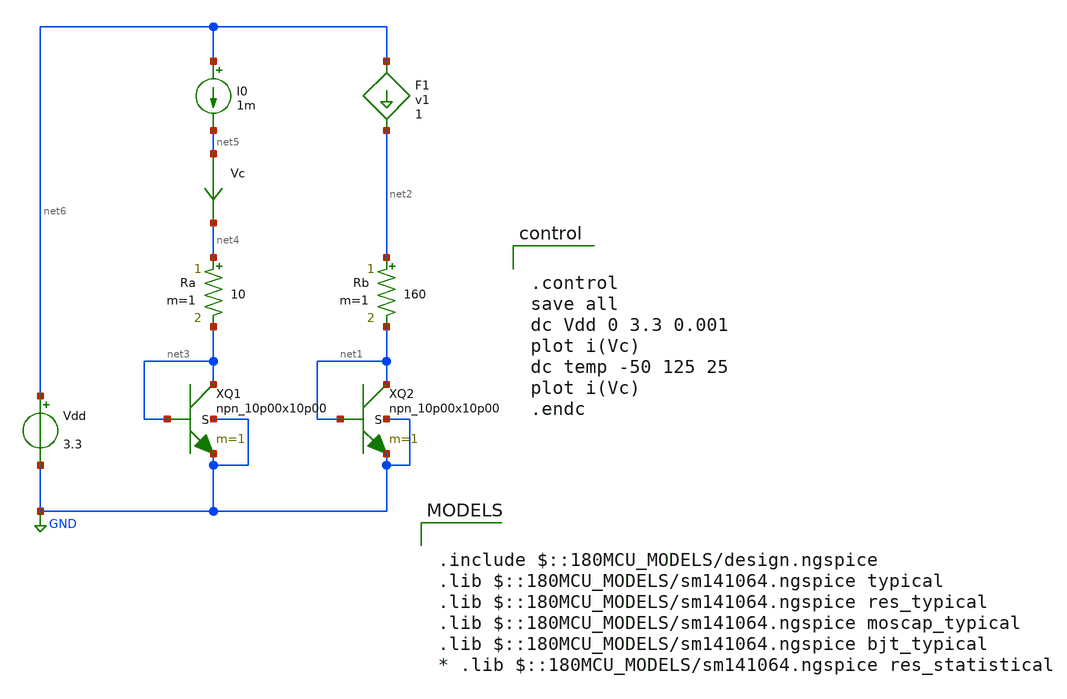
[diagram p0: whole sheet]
** sch_path: npn-diode-delta-1-03v3.sch
**.subckt npn-diode-delta-1-03v3
Vdd net6 GND 3.3
Vc net5 net4 0
.save i(vc)
XQ1 net3 net3 GND GND npn_10p00x10p00 m=1
XQ2 net1 net1 GND GND npn_10p00x10p00 m=1
Ra net4 net3 10 m=1
Rb net2 net1 160 m=1
F1 net6 net2 v1 1
I0 net6 net5 1m
**** begin user architecture code

.include $::180MCU_MODELS/design.ngspice
.lib $::180MCU_MODELS/sm141064.ngspice typical
.lib $::180MCU_MODELS/sm141064.ngspice res_typical
.lib $::180MCU_MODELS/sm141064.ngspice moscap_typical
.lib $::180MCU_MODELS/sm141064.ngspice bjt_typical
* .lib $::180MCU_MODELS/sm141064.ngspice res_statistical



.control
save all
dc Vdd 0 3.3 0.001
plot i(Vc)
dc temp -50 125 25
plot i(Vc)
.endc


**** end user architecture code
**.ends
.GLOBAL GND
.end
